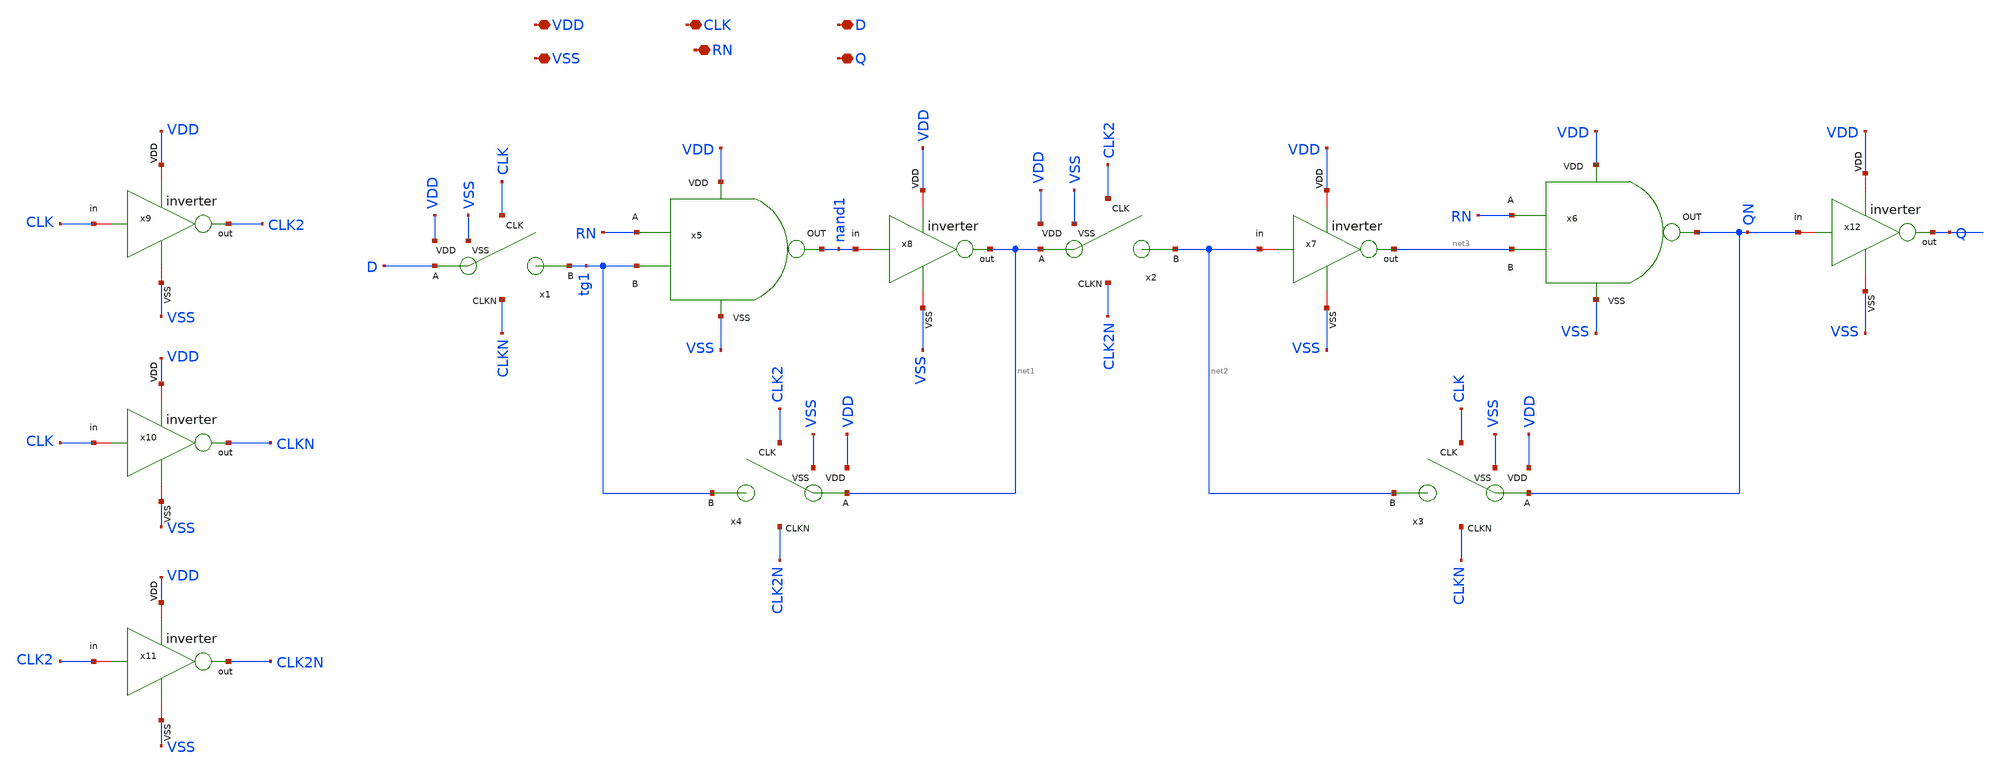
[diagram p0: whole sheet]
** sch_path: designs/sar_adc/digital/flip_flop/xschem/FF_D.sch
**.subckt FF_D VDD VSS CLK D Q RN
*.iopin VDD
*.iopin VSS
*.iopin CLK
*.iopin D
*.iopin Q
*.iopin RN
x1 CLK D VDD tg1 CLKN VSS TG
x2 CLK2 net1 VDD net2 CLK2N VSS TG
x3 CLK QN VDD net2 CLKN VSS TG
x4 CLK2 net1 VDD tg1 CLK2N VSS TG
x5 VDD VSS RN tg1 nand1 NAND
x6 VDD VSS RN net3 QN NAND
x8 VDD nand1 net1 VSS inverter
x9 VDD CLK CLK2 VSS inverter
x7 VDD net2 net3 VSS inverter
x10 VDD CLK CLKN VSS inverter
x11 VDD CLK2 CLK2N VSS inverter
x12 VDD QN Q VSS inverter
**.ends

* expanding   symbol:  sar_adc/digital/TG/xschem/TG.sym # of pins=6
** sym_path: designs/sar_adc/digital/TG/xschem/TG.sym
** sch_path: designs/sar_adc/digital/TG/xschem/TG.sch
.subckt TG CLK A VDD B CLKN VSS
*.iopin VDD
*.iopin VSS
*.ipin CLK
*.ipin CLKN
*.iopin A
*.iopin B
XM1 A CLK B VSS nfet_03v3 L=0.28u W=0.22u nf=1 ad='int((nf+1)/2) * W/nf * 0.18u' as='int((nf+2)/2) * W/nf * 0.18u'
+ pd='2*int((nf+1)/2) * (W/nf + 0.18u)' ps='2*int((nf+2)/2) * (W/nf + 0.18u)' nrd='0.18u / W' nrs='0.18u / W'
+ sa=0 sb=0 sd=0 m=1
XM2 A CLKN B VDD pfet_03v3 L=0.28u W=0.22u nf=1 ad='int((nf+1)/2) * W/nf * 0.18u' as='int((nf+2)/2) * W/nf * 0.18u'
+ pd='2*int((nf+1)/2) * (W/nf + 0.18u)' ps='2*int((nf+2)/2) * (W/nf + 0.18u)' nrd='0.18u / W' nrs='0.18u / W'
+ sa=0 sb=0 sd=0 m=1
.ends


* expanding   symbol:  sar_adc/digital/NAND/xschem/NAND.sym # of pins=5
** sym_path: designs/sar_adc/digital/NAND/xschem/NAND.sym
** sch_path: designs/sar_adc/digital/NAND/xschem/NAND.sch
.subckt NAND VDD VSS A B out
*.iopin VDD
*.iopin A
*.iopin B
*.iopin out
*.iopin VSS
x1 VDD net1 net2 VSS inverter
x2 VDD net2 out VSS inverter
XM2 net1 A VDD VDD pfet_03v3 L=0.28u W=0.22u nf=1 ad='int((nf+1)/2) * W/nf * 0.18u' as='int((nf+2)/2) * W/nf * 0.18u'
+ pd='2*int((nf+1)/2) * (W/nf + 0.18u)' ps='2*int((nf+2)/2) * (W/nf + 0.18u)' nrd='0.18u / W' nrs='0.18u / W'
+ sa=0 sb=0 sd=0 m=1
XM1 net1 A net3 VSS nfet_03v3 L=0.28u W=0.22u nf=1 ad='int((nf+1)/2) * W/nf * 0.18u' as='int((nf+2)/2) * W/nf * 0.18u'
+ pd='2*int((nf+1)/2) * (W/nf + 0.18u)' ps='2*int((nf+2)/2) * (W/nf + 0.18u)' nrd='0.18u / W' nrs='0.18u / W'
+ sa=0 sb=0 sd=0 m=1
XM3 net1 B VDD VDD pfet_03v3 L=0.28u W=0.22u nf=1 ad='int((nf+1)/2) * W/nf * 0.18u' as='int((nf+2)/2) * W/nf * 0.18u'
+ pd='2*int((nf+1)/2) * (W/nf + 0.18u)' ps='2*int((nf+2)/2) * (W/nf + 0.18u)' nrd='0.18u / W' nrs='0.18u / W'
+ sa=0 sb=0 sd=0 m=1
XM4 net3 B VSS VSS nfet_03v3 L=0.28u W=0.22u nf=1 ad='int((nf+1)/2) * W/nf * 0.18u' as='int((nf+2)/2) * W/nf * 0.18u'
+ pd='2*int((nf+1)/2) * (W/nf + 0.18u)' ps='2*int((nf+2)/2) * (W/nf + 0.18u)' nrd='0.18u / W' nrs='0.18u / W'
+ sa=0 sb=0 sd=0 m=1
.ends


* expanding   symbol:  sar_adc/digital/inverter/xschem/inverter.sym # of pins=6
** sym_path: designs/sar_adc/digital/inverter/xschem/inverter.sym
** sch_path: designs/sar_adc/digital/inverter/xschem/inverter.sch
.subckt inverter VDD in out VSS
*.opin out
*.iopin in
*.iopin VDD
*.iopin VSS
XM1 out in VSS VSS nfet_03v3 L=0.28u W=1u nf=1 ad='int((nf+1)/2) * W/nf * 0.18u' as='int((nf+2)/2) * W/nf * 0.18u'
+ pd='2*int((nf+1)/2) * (W/nf + 0.18u)' ps='2*int((nf+2)/2) * (W/nf + 0.18u)' nrd='0.18u / W' nrs='0.18u / W'
+ sa=0 sb=0 sd=0 m=1
XM2 out in VDD VDD pfet_03v3 L=0.28u W=3u nf=1 ad='int((nf+1)/2) * W/nf * 0.18u' as='int((nf+2)/2) * W/nf * 0.18u'
+ pd='2*int((nf+1)/2) * (W/nf + 0.18u)' ps='2*int((nf+2)/2) * (W/nf + 0.18u)' nrd='0.18u / W' nrs='0.18u / W'
+ sa=0 sb=0 sd=0 m=1
.ends

.end
